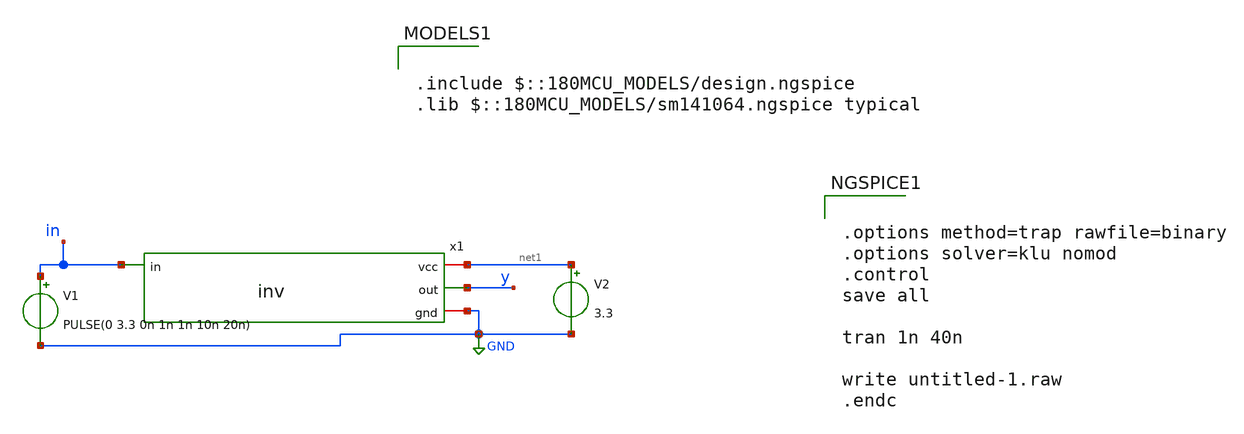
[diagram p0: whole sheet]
** sch_path: designs/schematics/mux2x1/inv_tb.sch
**.subckt inv_tb
V1 in GND PULSE(0 3.3 0n 1n 1n 10n 20n)
V2 net1 GND 3.3
x1 net1 in y GND inv
**** begin user architecture code


.options method=trap rawfile=binary
.options solver=klu nomod
.control
save all

tran 1n 40n

write untitled-1.raw
.endc



.include $::180MCU_MODELS/design.ngspice
.lib $::180MCU_MODELS/sm141064.ngspice typical

**** end user architecture code
**.ends

* expanding   symbol:  voidwalkers-scandff-gf180mcu/designs/schematics/mux2x1/inv.sym # of pins=4
** sym_path: designs/schematics/mux2x1/inv.sym
** sch_path: designs/schematics/mux2x1/inv.sch
.subckt inv vcc in out gnd
*.ipin in
*.opin out
*.iopin vcc
*.iopin gnd
XM2 out in vcc vcc pfet_03v3 L=0.28u W=0.22u nf=1 ad='int((nf+1)/2) * W/nf * 0.18u' as='int((nf+2)/2) * W/nf * 0.18u'
+ pd='2*int((nf+1)/2) * (W/nf + 0.18u)' ps='2*int((nf+2)/2) * (W/nf + 0.18u)' nrd='0.18u / W' nrs='0.18u / W'
+ sa=0 sb=0 sd=0 m=1
XM1 out in gnd gnd nfet_03v3 L=0.28u W=0.22u nf=1 ad='int((nf+1)/2) * W/nf * 0.18u' as='int((nf+2)/2) * W/nf * 0.18u'
+ pd='2*int((nf+1)/2) * (W/nf + 0.18u)' ps='2*int((nf+2)/2) * (W/nf + 0.18u)' nrd='0.18u / W' nrs='0.18u / W'
+ sa=0 sb=0 sd=0 m=1
.ends

.GLOBAL GND
.end
